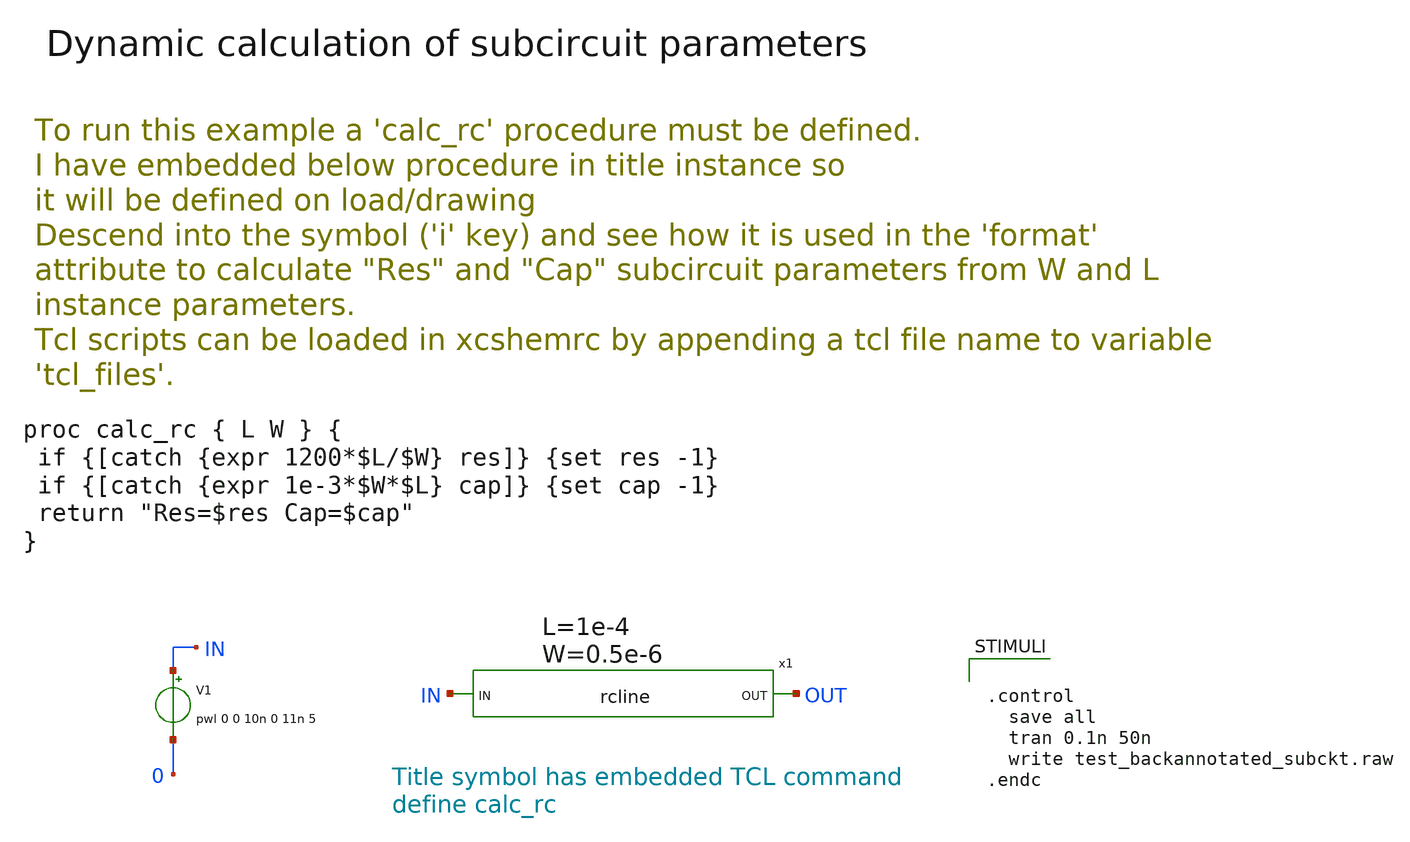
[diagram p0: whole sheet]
** sch_path: xschem-src/xschem_library/examples/test_backannotated_subckt.sch
* Copyright (C) 1998-2026 Stefan Frederik Schippers
* This program is free software; you can redistribute it and/or modify
* it under the terms of the GNU General Public License as published by
* the Free Software Foundation; either version 2 of the License, or
* (at your option) any later version.
* This program is distributed in the hope that it will be useful,
* but WITHOUT ANY WARRANTY; without even the implied warranty of
* MERCHANTABILITY or FITNESS FOR A PARTICULAR PURPOSE.  See the
* GNU General Public License for more details.
* You should have received a copy of the GNU General Public License
* along with this program; if not, write to the Free Software
**.subckt test_backannotated_subckt
V1 IN 0 pwl 0 0 10n 0 11n 5
x1 OUT IN rcline [ calc_rc 1e-4 0.5e-6 ]
**** begin user architecture code


.control
  save all
  tran 0.1n 50n
  write test_backannotated_subckt.raw
.endc


**** end user architecture code
**.ends

* expanding   symbol:  rcline.sym # of pins=2
** sym_path: xschem-src/xschem_library/examples/rcline.sym
** sch_path: xschem-src/xschem_library/examples/rcline.sch
.subckt rcline OUT IN  Res=1e4 Cap=1e-6
*.ipin IN
*.opin OUT
C1 net1 0 'Cap/2' m=1
R1 net1 OUT 'Res/2' m=1
R2 IN net1 'Res/2' m=1
.ends

.end
